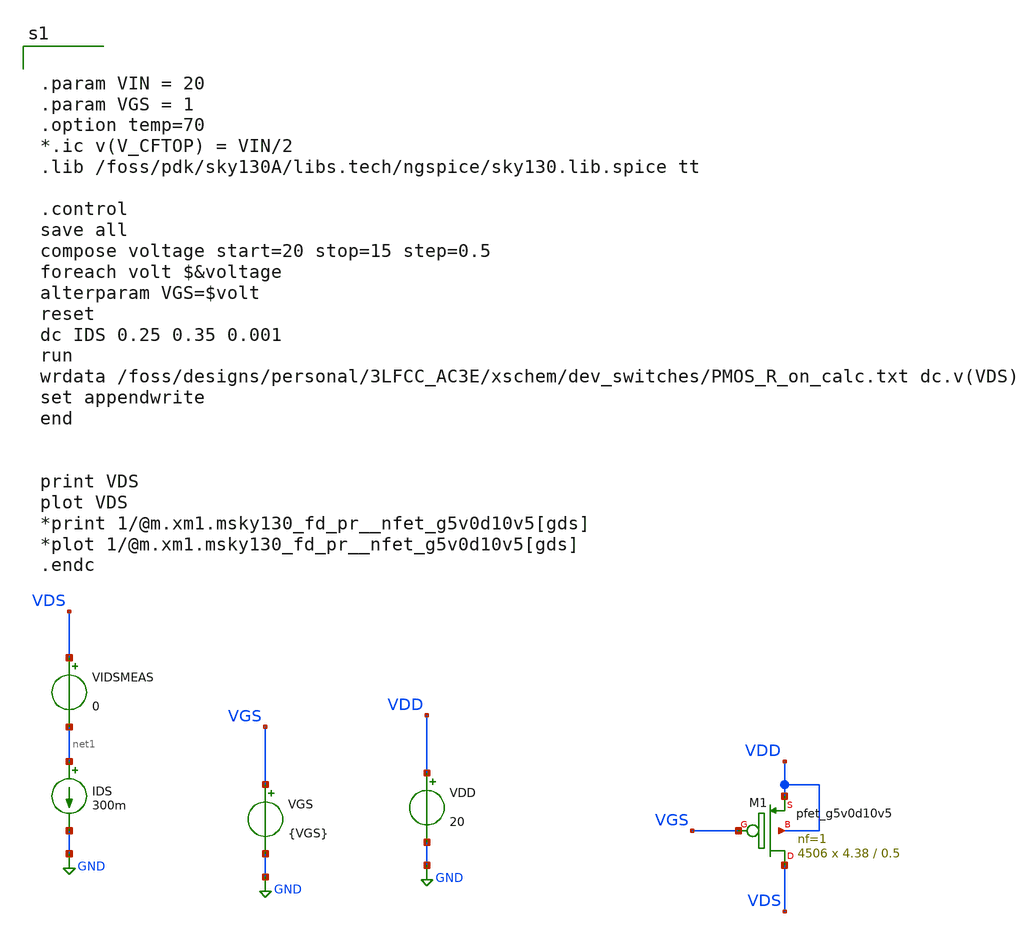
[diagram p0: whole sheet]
** sch_path: Notebooks/3LFCC/PMOS_allfingers_RONcalc_v2p2_vicente.sch
**.subckt PMOS_allfingers_RONcalc_v2p2_vicente
VGS VGS GND {VGS}
IDS net1 GND 300m
VIDSMEAS VDS net1 0
XM1 VDS VGS VDD VDD sky130_fd_pr__pfet_g5v0d10v5 L=0.5 W=4.38 nf=1 ad='int((nf+1)/2) * W/nf * 0.29' as='int((nf+2)/2) * W/nf * 0.29'
+ pd='2*int((nf+1)/2) * (W/nf + 0.29)' ps='2*int((nf+2)/2) * (W/nf + 0.29)' nrd='0.29 / W' nrs='0.29 / W'
+ sa=0 sb=0 sd=0 mult=4506 m=4506
VDD VDD GND 20
**** begin user architecture code


.param VIN = 20
.param VGS = 1
.option temp=70
*.ic v(V_CFTOP) = VIN/2
.lib /foss/pdk/sky130A/libs.tech/ngspice/sky130.lib.spice tt

.control
save all
compose voltage start=20 stop=15 step=0.5
foreach volt $&voltage
alterparam VGS=$volt
reset
dc IDS 0.25 0.35 0.001
run
wrdata /foss/designs/personal/3LFCC_AC3E/xschem/dev_switches/PMOS_R_on_calc.txt dc.v(VDS)
set appendwrite
end


print VDS
plot VDS
*print 1/@m.xm1.msky130_fd_pr__nfet_g5v0d10v5[gds]
*plot 1/@m.xm1.msky130_fd_pr__nfet_g5v0d10v5[gds]
.endc



**** end user architecture code
**.ends
.GLOBAL GND
.end
